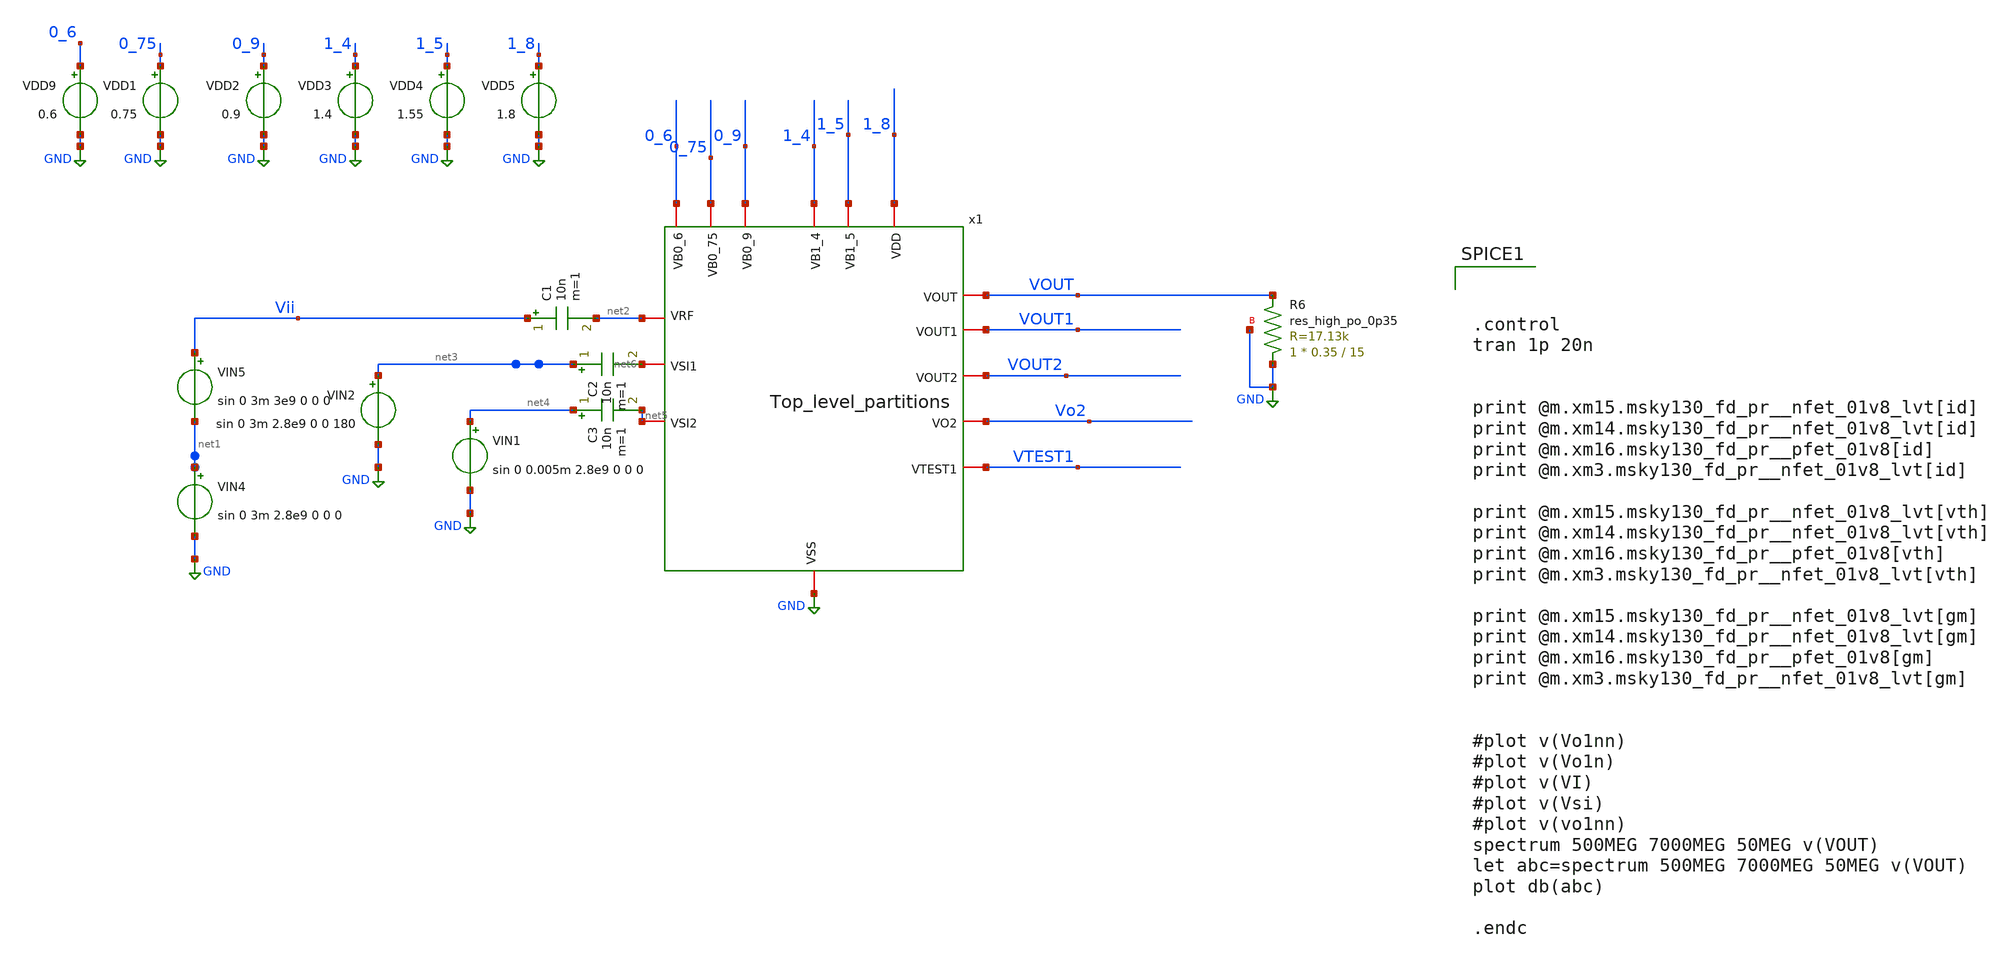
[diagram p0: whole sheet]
** sch_path: xschem/xschem4_sic_oct_20/Top_level_partitions_tb_tran.sch
**.subckt Top_level_partitions_tb_tran
x1 1_5 1_8 VOUT2 VOUT1 0_6 0_75 0_9 VOUT net2 net5 1_4 VTEST1 net6 GND Vo2 Top_level_partitions
VDD9 0_6 GND 0.6
VDD1 0_75 GND 0.75
VDD2 0_9 GND 0.9
VDD3 1_4 GND 1.4
VDD4 1_5 GND 1.55
VDD5 1_8 GND 1.8
XR6 GND VOUT GND sky130_fd_pr__res_high_po_0p35 L=15 mult=1 m=1
C1 Vii net2 10n m=1
VIN4 net1 GND sin 0 3m 2.8e9 0 0 0
VIN5 Vii net1 sin 0 3m 3e9 0 0 0
VIN2 net3 GND sin 0 3m 2.8e9 0 0 180
C2 net3 net6 10n m=1
VIN1 net4 GND sin 0 0.005m 2.8e9 0 0 0
C3 net4 net5 10n m=1
**** begin user architecture code

.lib $::SKYWATER_MODELS/sky130.lib.spice fs




.control
tran 1p 20n


print @m.xm15.msky130_fd_pr__nfet_01v8_lvt[id]
print @m.xm14.msky130_fd_pr__nfet_01v8_lvt[id]
print @m.xm16.msky130_fd_pr__pfet_01v8[id]
print @m.xm3.msky130_fd_pr__nfet_01v8_lvt[id]

print @m.xm15.msky130_fd_pr__nfet_01v8_lvt[vth]
print @m.xm14.msky130_fd_pr__nfet_01v8_lvt[vth]
print @m.xm16.msky130_fd_pr__pfet_01v8[vth]
print @m.xm3.msky130_fd_pr__nfet_01v8_lvt[vth]

print @m.xm15.msky130_fd_pr__nfet_01v8_lvt[gm]
print @m.xm14.msky130_fd_pr__nfet_01v8_lvt[gm]
print @m.xm16.msky130_fd_pr__pfet_01v8[gm]
print @m.xm3.msky130_fd_pr__nfet_01v8_lvt[gm]


#plot v(Vo1nn)
#plot v(Vo1n)
#plot v(VI)
#plot v(Vsi)
#plot v(vo1nn)
spectrum 500MEG 7000MEG 50MEG v(VOUT)
let abc=spectrum 500MEG 7000MEG 50MEG v(VOUT)
plot db(abc)

.endc


**** end user architecture code
**.ends

* expanding   symbol:  Top_level_partitions.sym # of pins=15
** sym_path: xschem/xschem4_sic_oct_20/Top_level_partitions.sym
** sch_path: xschem/xschem4_sic_oct_20/Top_level_partitions.sch
.subckt Top_level_partitions VB1_5 VDD VOUT2 VOUT1 VB0_6 VB0_75 VB0_9 VOUT VRF VSI2 VB1_4 VTEST1
+ VSI1 VSS VO2
*.iopin VDD
*.iopin VSS
*.iopin VB1_5
*.iopin VRF
*.iopin VB1_4
*.iopin VB0_75
*.iopin VSI1
*.iopin VB0_9
*.iopin VB0_6
*.iopin VSI2
*.iopin VOUT
*.iopin VTEST1
*.iopin VOUT2
*.iopin VOUT1
*.iopin VO2
x1 VOUT1 VDD VB1_4 VTEST1 VRF VSI1 VB0_75 VSS partition1
x2 VOUT2 VDD VOUT1 VSS VB1_5 VRF partition2
x3 VDD VOUT2 VO2 VOUT1 VSS VB0_9 partition3
x4 VDD VB0_6 VO2 VSI2 VSS VB0_75 partition4
x5 VDD VO2 VOUT VSS partition5
.ends


* expanding   symbol:  partition1.sym # of pins=8
** sym_path: xschem/xschem4_sic_oct_20/partition1.sym
** sch_path: xschem/xschem4_sic_oct_20/partition1.sch
.subckt partition1 VOUT1 VDD VB1_4 VTEST1 VRF VSI1 VB0_75 VSS
*.iopin VRF
*.iopin VSS
*.iopin VB0_75
*.iopin VSI1
*.iopin VB1_4
*.iopin VTEST1
*.iopin VOUT1
*.iopin VDD
XM12 VTEST1 VRF VSS VSS sky130_fd_pr__nfet_01v8_lvt L=0.15 W=220 nf=22 ad='int((nf+1)/2) * W/nf * 0.29'
+ as='int((nf+2)/2) * W/nf * 0.29' pd='2*int((nf+1)/2) * (W/nf + 0.29)' ps='2*int((nf+2)/2) * (W/nf + 0.29)'
+ nrd='0.29 / W' nrs='0.29 / W' sa=0 sb=0 sd=0 mult=1 m=1
XM13 VTEST1 VRF VDD VDD sky130_fd_pr__pfet_01v8 L=0.15 W=30 nf=3 ad='int((nf+1)/2) * W/nf * 0.29' as='int((nf+2)/2) * W/nf * 0.29'
+ pd='2*int((nf+1)/2) * (W/nf + 0.29)' ps='2*int((nf+2)/2) * (W/nf + 0.29)' nrd='0.29 / W' nrs='0.29 / W'
+ sa=0 sb=0 sd=0 mult=1 m=1
XM14 VOUT1 VB1_4 VTEST1 VSS sky130_fd_pr__nfet_01v8_lvt L=0.15 W=80 nf=8 ad='int((nf+1)/2) * W/nf * 0.29'
+ as='int((nf+2)/2) * W/nf * 0.29' pd='2*int((nf+1)/2) * (W/nf + 0.29)' ps='2*int((nf+2)/2) * (W/nf + 0.29)'
+ nrd='0.29 / W' nrs='0.29 / W' sa=0 sb=0 sd=0 mult=1 m=1
XM16 VRF VB0_75 VSS VSS sky130_fd_pr__nfet_01v8_lvt L=0.15 W=7.8 nf=1 ad='int((nf+1)/2) * W/nf * 0.29'
+ as='int((nf+2)/2) * W/nf * 0.29' pd='2*int((nf+1)/2) * (W/nf + 0.29)' ps='2*int((nf+2)/2) * (W/nf + 0.29)'
+ nrd='0.29 / W' nrs='0.29 / W' sa=0 sb=0 sd=0 mult=1 m=1
XM20 VTEST1 VSI1 VSS VSS sky130_fd_pr__nfet_01v8_lvt L=0.15 W=240 nf=24 ad='int((nf+1)/2) * W/nf * 0.29'
+ as='int((nf+2)/2) * W/nf * 0.29' pd='2*int((nf+1)/2) * (W/nf + 0.29)' ps='2*int((nf+2)/2) * (W/nf + 0.29)'
+ nrd='0.29 / W' nrs='0.29 / W' sa=0 sb=0 sd=0 mult=1 m=1
XR16 VB0_75 VSI1 VSS sky130_fd_pr__res_high_po_0p35 L=6.2 mult=1 m=1
.ends


* expanding   symbol:  partition2.sym # of pins=6
** sym_path: xschem/xschem4_sic_oct_20/partition2.sym
** sch_path: xschem/xschem4_sic_oct_20/partition2.sch
.subckt partition2 VOUT2 VDD VOUT1 VSS VB1_5 VRF
*.iopin VDD
*.iopin VOUT1
*.iopin VOUT2
*.iopin VB1_5
*.iopin VSS
*.iopin VRF
XR4 VB1_5 net1 VSS sky130_fd_pr__res_high_po_0p35 L=4 mult=1 m=1
XC5 net1 VOUT1 sky130_fd_pr__cap_mim_m3_2 W=30 L=30 MF=1 m=1
XM15 net2 net1 VRF VSS sky130_fd_pr__nfet_01v8_lvt L=0.15 W=7.8 nf=1 ad='int((nf+1)/2) * W/nf * 0.29'
+ as='int((nf+2)/2) * W/nf * 0.29' pd='2*int((nf+1)/2) * (W/nf + 0.29)' ps='2*int((nf+2)/2) * (W/nf + 0.29)'
+ nrd='0.29 / W' nrs='0.29 / W' sa=0 sb=0 sd=0 mult=1 m=1
XR14 net2 VDD VSS sky130_fd_pr__res_high_po_0p35 L=0.5 mult=1 m=1
XR15 VOUT1 VDD VSS sky130_fd_pr__res_high_po_0p69 L=0.69 mult=8 m=8
XM21 VOUT2 VOUT1 VSS VSS sky130_fd_pr__nfet_01v8_lvt L=0.15 W=7.8 nf=1 ad='int((nf+1)/2) * W/nf * 0.29'
+ as='int((nf+2)/2) * W/nf * 0.29' pd='2*int((nf+1)/2) * (W/nf + 0.29)' ps='2*int((nf+2)/2) * (W/nf + 0.29)'
+ nrd='0.29 / W' nrs='0.29 / W' sa=0 sb=0 sd=0 mult=1 m=1
XR17 VOUT2 VDD VSS sky130_fd_pr__res_high_po_0p35 L=0.5 mult=1 m=1
.ends


* expanding   symbol:  partition3.sym # of pins=6
** sym_path: xschem/xschem4_sic_oct_20/partition3.sym
** sch_path: xschem/xschem4_sic_oct_20/partition3.sch
.subckt partition3 VDD VOUT2 Vo2 VOUT1 VSS VB0_9
*.iopin VB0_9
*.iopin VDD
*.iopin VSS
*.iopin VOUT2
*.iopin VOUT1
*.iopin Vo2
XM17 Vo2 net2 VSS VSS sky130_fd_pr__nfet_01v8_lvt L=0.15 W=45 nf=7 ad='int((nf+1)/2) * W/nf * 0.29' as='int((nf+2)/2) * W/nf * 0.29'
+ pd='2*int((nf+1)/2) * (W/nf + 0.29)' ps='2*int((nf+2)/2) * (W/nf + 0.29)' nrd='0.29 / W' nrs='0.29 / W'
+ sa=0 sb=0 sd=0 mult=1 m=1
XM18 VDD net1 Vo2 VSS sky130_fd_pr__nfet_01v8_lvt L=0.15 W=12 nf=3 ad='int((nf+1)/2) * W/nf * 0.29' as='int((nf+2)/2) * W/nf * 0.29'
+ pd='2*int((nf+1)/2) * (W/nf + 0.29)' ps='2*int((nf+2)/2) * (W/nf + 0.29)' nrd='0.29 / W' nrs='0.29 / W'
+ sa=0 sb=0 sd=0 mult=1 m=1
XR11 net1 VDD VSS sky130_fd_pr__res_high_po_0p35 L=15 mult=1 m=1
XC7 VOUT2 net1 sky130_fd_pr__cap_mim_m3_2 W=30 L=30 MF=1 m=1
XR12 VB0_9 net2 VSS sky130_fd_pr__res_high_po_0p35 L=8 mult=1 m=1
XC8 VOUT1 net2 sky130_fd_pr__cap_mim_m3_2 W=30 L=30 MF=1 m=1
XD1 VSS net1 sky130_fd_pr__diode_pw2nd_05v5 area=1e12 pj=4e6
.ends


* expanding   symbol:  partition4.sym # of pins=6
** sym_path: xschem/xschem4_sic_oct_20/partition4.sym
** sch_path: xschem/xschem4_sic_oct_20/partition4.sch
.subckt partition4 VDD VB0_6 V02 VSI2 VSS VB0_75
*.iopin VSI2
*.iopin VB0_6
*.iopin VDD
*.iopin VSS
*.iopin VB0_75
*.iopin V02
XM19 V02 net1 VDD VDD sky130_fd_pr__pfet_01v8 L=0.15 W=30 nf=3 ad='int((nf+1)/2) * W/nf * 0.29' as='int((nf+2)/2) * W/nf * 0.29'
+ pd='2*int((nf+1)/2) * (W/nf + 0.29)' ps='2*int((nf+2)/2) * (W/nf + 0.29)' nrd='0.29 / W' nrs='0.29 / W'
+ sa=0 sb=0 sd=0 mult=1 m=1
XR13 VB0_6 net1 VSS sky130_fd_pr__res_high_po_0p35 L=6.2 mult=1 m=1
XM22 V02 VSI2 VSS VSS sky130_fd_pr__nfet_01v8_lvt L=0.15 W=80 nf=8 ad='int((nf+1)/2) * W/nf * 0.29' as='int((nf+2)/2) * W/nf * 0.29'
+ pd='2*int((nf+1)/2) * (W/nf + 0.29)' ps='2*int((nf+2)/2) * (W/nf + 0.29)' nrd='0.29 / W' nrs='0.29 / W'
+ sa=0 sb=0 sd=0 mult=1 m=1
XR18 VB0_75 VSI2 VSS sky130_fd_pr__res_high_po_0p35 L=0.5 mult=1 m=1
.ends


* expanding   symbol:  partition5.sym # of pins=4
** sym_path: xschem/xschem4_sic_oct_20/partition5.sym
** sch_path: xschem/xschem4_sic_oct_20/partition5.sch
.subckt partition5 VDD VO2 VOUT VSS
*.iopin VOUT
*.iopin VDD
*.iopin VSS
*.iopin VO2
XM4 VDD net1 VOUT VSS sky130_fd_pr__nfet_01v8_lvt L=0.15 W=100 nf=10 ad='int((nf+1)/2) * W/nf * 0.29'
+ as='int((nf+2)/2) * W/nf * 0.29' pd='2*int((nf+1)/2) * (W/nf + 0.29)' ps='2*int((nf+2)/2) * (W/nf + 0.29)'
+ nrd='0.29 / W' nrs='0.29 / W' sa=0 sb=0 sd=0 mult=1 m=1
XR5 net1 VDD VSS sky130_fd_pr__res_high_po_0p35 L=4 mult=1 m=1
XR6 VSS VOUT VSS sky130_fd_pr__res_high_po_0p35 L=15 mult=1 m=1
XC3 VO2 net1 sky130_fd_pr__cap_mim_m3_2 W=30 L=30 MF=1 m=1
.ends

.GLOBAL GND
.end
